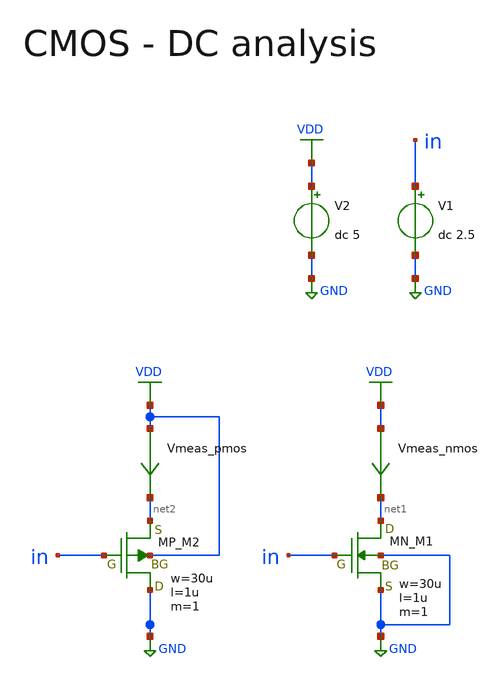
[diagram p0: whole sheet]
** sch_path: member_project/AM_Radio/Yamada3/xschem/tb_cmos_dc.sch
**.subckt tb_cmos_dc
V2 VDD GND dc 5
V1 in GND dc 2.5
XM1 net1 in GND GND NMOS w=30u l=1u as=0 ad=0 ps=0 pd=0 nrd=0 nrs=0 m=1
Vmeas_nmos VDD net1 0
.save i(vmeas_nmos)
Vmeas_pmos VDD net2 0
.save i(vmeas_pmos)
XM2 GND in net2 VDD PMOS w=30u l=1u as=0 ad=0 ps=0 pd=0 nrd=0 nrs=0 m=1
**** begin user architecture code

.option savecurrent
.param nmos_w = 10u
.control
save all
# DC analysis
dc v1  0  5 1m
let gm_nmos= deriv(i(vmeas_nmos))
let gm_pmos= deriv(i(vmeas_pmos))
let gmid_nmos= gm_nmos/i(vmeas_nmos)
let gmid_pmos= gm_pmos/i(vmeas_pmos)
let ft_nmos=abs(gm_nmos/(2*pi*@m.xm1.m1[cgg]))
let ft_pmos=abs(gm_pmos/(2*pi*@m.xm2.m1[cgg]))
let rout_nmos=abs(v(vdd)/i(vmeas_nmos))
let rout_pmos=abs(v(vdd)/i(vmeas_pmos))
show
print @m.xm1.m1[vth]
print @m.xm2.m1[vth]
write tb_cmos_dc.raw all
.endc

 .include $::LIB/ip62_models
**** end user architecture code
**.ends
.GLOBAL GND
.GLOBAL VDD
.end
